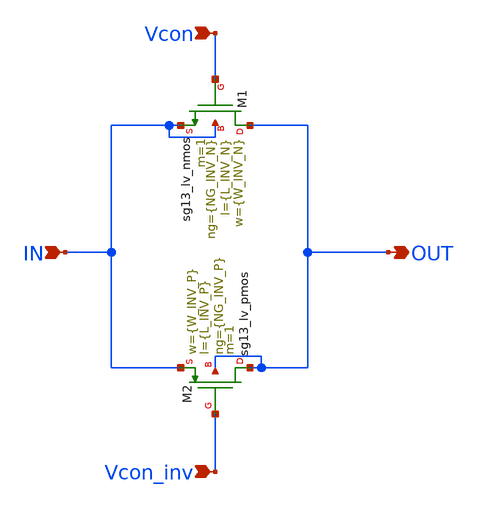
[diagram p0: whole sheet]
** sch_path: designs/archives/fine_gain/untitled.sch
**.subckt untitled IN OUT Vcon Vcon_inv
*.ipin IN
*.opin OUT
*.ipin Vcon
*.ipin Vcon_inv
XM1 OUT Vcon IN IN sg13_lv_nmos w={W_INV_N} l={L_INV_N} ng={NG_INV_N} m=1 mm_ok=1
XM2 OUT Vcon_inv IN OUT sg13_lv_pmos w={W_INV_P} l={L_INV_P} ng={NG_INV_P} m=1 mm_ok=1
**.ends
.end
